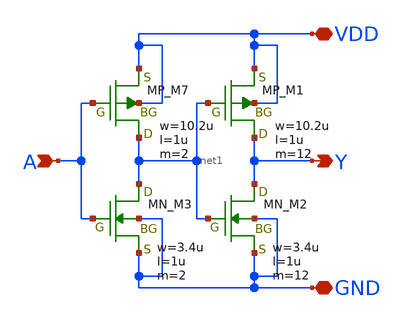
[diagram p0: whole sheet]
** sch_path: libs.tech/xschem/TR-1um_5_stdcell/BUF_X12.sch
**.subckt BUF_X12 A Y VDD GND
*.ipin A
*.opin Y
*.iopin VDD
*.iopin GND
XM7 net1 A VDD VDD PMOS w=10.2u l=1u nrd=0 nrs=0 m=2
XM1 Y net1 VDD VDD PMOS w=10.2u l=1u nrd=0 nrs=0 m=12
XM3 net1 A GND GND NMOS w=3.4u l=1u nrd=0 nrs=0 m=2
XM2 Y net1 GND GND NMOS w=3.4u l=1u nrd=0 nrs=0 m=12
**.ends
.end
